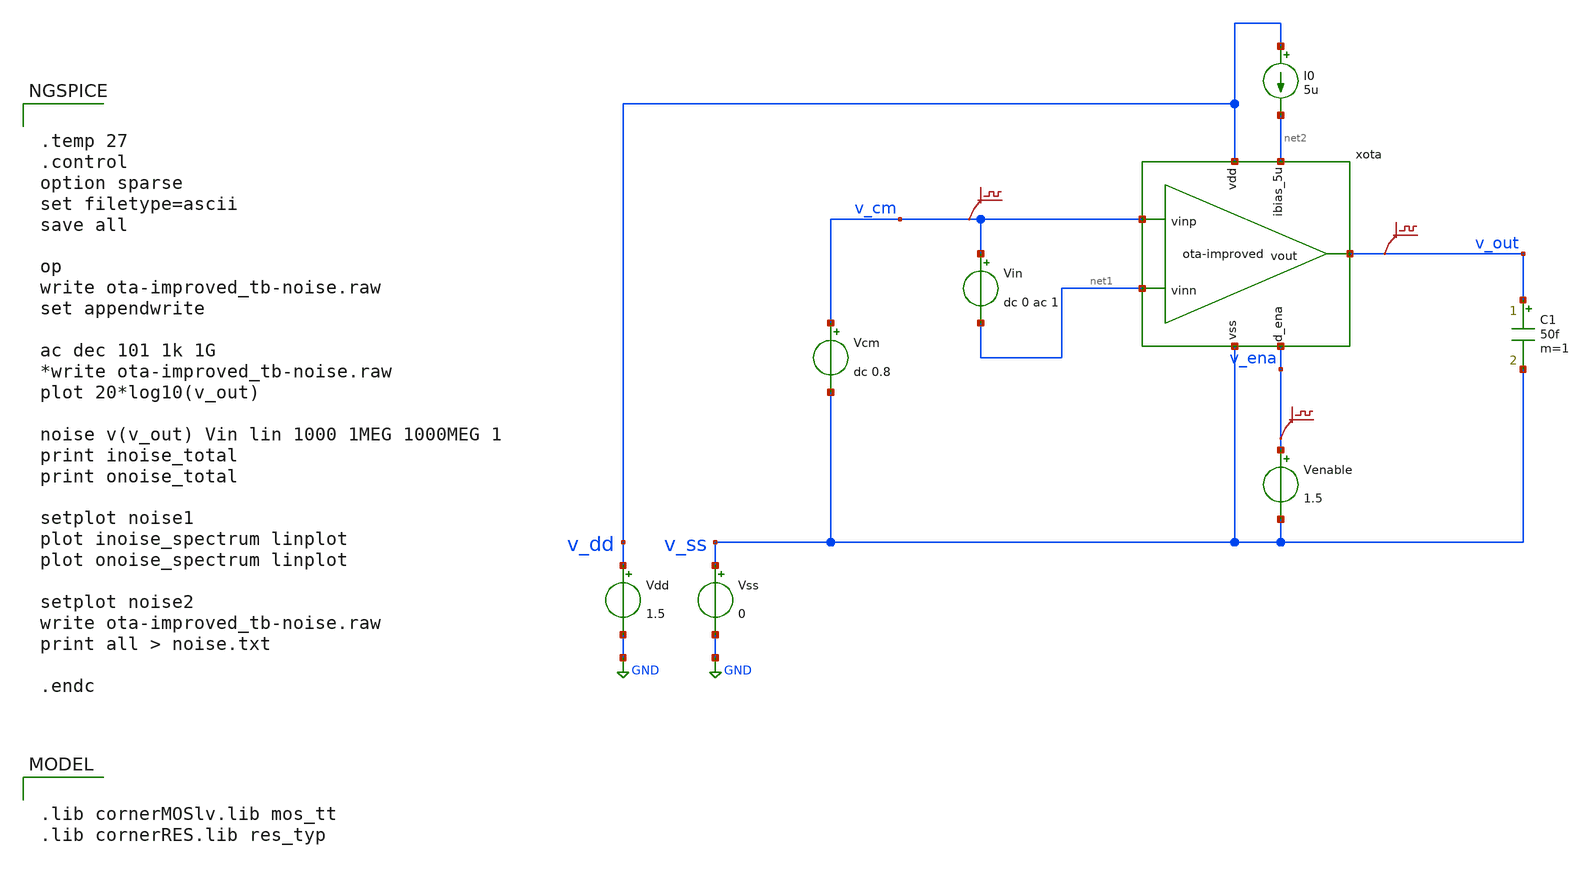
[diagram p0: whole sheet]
** sch_path: xschem/ota-improved_tb-noise.sch
* (c) 2024-2025 Harald Pretl, Apache-2.0 license
**.subckt ota-improved_tb-noise
Vdd v_dd GND 1.5
xota v_dd v_out v_cm net1 net2 v_ena v_ss ota-improved
Vss v_ss GND 0
C1 v_out v_ss 50f m=1
Vcm v_cm v_ss dc 0.8
I0 v_dd net2 5u
Venable v_ena v_ss 1.5
.save v(v_cm)
.save v(v_out)
.save v(v_ena)
Vin v_cm net1 dc 0 ac 1
**** begin user architecture code

.lib cornerMOSlv.lib mos_tt
.lib cornerRES.lib res_typ



.temp 27
.control
option sparse
set filetype=ascii
save all

op
write ota-improved_tb-noise.raw
set appendwrite

ac dec 101 1k 1G
*write ota-improved_tb-noise.raw
plot 20*log10(v_out)

noise v(v_out) Vin lin 1000 1MEG 1000MEG 1
print inoise_total
print onoise_total

setplot noise1
plot inoise_spectrum linplot
plot onoise_spectrum linplot

setplot noise2
write ota-improved_tb-noise.raw
print all > noise.txt

.endc


**** end user architecture code
**.ends

* expanding   symbol:  ota-improved.sym # of pins=7
** sym_path: xschem/ota-improved.sym
** sch_path: xschem/ota-improved.sch
.subckt ota-improved vdd vout vinp vinn ibias_5u d_ena vss
*.ipin ibias_5u
*.iopin vdd
*.iopin vss
*.ipin vinp
*.ipin vinn
*.opin vout
*.ipin d_ena
XM5 net7 gate vss vss sg13_lv_nmos w=6u l=5u ng=3 m=1 mm_ok=1
XM4 net2 gate_p vdd vdd sg13_lv_pmos w=3u l=0.5u ng=1 m=1 mm_ok=1
XM1 net5 vinp tail vss sg13_lv_nmos w=1u l=0.5u ng=1 m=1 mm_ok=1
XM2 net6 vinn tail vss sg13_lv_nmos w=1u l=0.5u ng=1 m=1 mm_ok=1
XM3 net3 gate_p vdd vdd sg13_lv_pmos w=3u l=0.5u ng=1 m=1 mm_ok=1
XM6 net1 gate vss vss sg13_lv_nmos w=2u l=5u ng=1 m=1 mm_ok=1
XMpd5 gate ena_n vss vss sg13_lv_nmos w=1u l=0.13u ng=1 m=1 mm_ok=1
XMpd3 ena ena_n vss vss sg13_lv_nmos w=1u l=0.13u ng=1 m=1 mm_ok=1
XMpd4 ena ena_n vdd vdd sg13_lv_pmos w=1u l=0.13u ng=1 m=1 mm_ok=1
XMpd6 net1 ena gate vss sg13_lv_nmos w=1u l=0.13u ng=1 m=1 mm_ok=1
XM2c vout dp_casc net6 vss sg13_lv_nmos w=1u l=0.5u ng=1 m=1 mm_ok=1
XM1c gate_p dp_casc net5 vss sg13_lv_nmos w=1u l=0.5u ng=1 m=1 mm_ok=1
XM4c vout gate_pc net2 vdd sg13_lv_pmos w=3u l=0.5u ng=1 m=1 mm_ok=1
XM3c gate_p gate_pc net3 vdd sg13_lv_pmos w=3u l=0.5u ng=1 m=1 mm_ok=1
XM7 net4 gate vss vss sg13_lv_nmos w=2u l=5u ng=1 m=1 mm_ok=1
XMpd8 gate_p ena vdd vdd sg13_lv_pmos w=1u l=0.13u ng=1 m=1 mm_ok=1
XM8_1 net8 gate_pc vdd vdd sg13_lv_pmos w=3u l=0.5u ng=1 m=1 mm_ok=1
XM9_1 net9 gate_pc vdd vdd sg13_lv_pmos w=3u l=0.5u ng=1 m=1 mm_ok=1
XMpd7 gate_pc ena vdd vdd sg13_lv_pmos w=1u l=0.13u ng=1 m=1 mm_ok=1
XM10_3 net10 dp_casc net11 vss sg13_lv_nmos w=1u l=0.5u ng=1 m=1 mm_ok=1
Vmeas gate_pc net4 0
.save i(vmeas)
Vmeas1 tail net7 0
.save i(vmeas1)
XMpd1 ena_n d_ena vss vss sg13_lv_nmos w=1u l=0.13u ng=1 m=1 mm_ok=1
XMpd2 ena_n d_ena vdd vdd sg13_lv_pmos w=1u l=0.13u ng=1 m=1 mm_ok=1
Vmeas4 ibias_5u net1 0
.save i(vmeas4)
XMpd11 vout ena_n vss vss sg13_lv_nmos w=0.5u l=0.13u ng=1 m=1 mm_ok=1
XM10_4 net11 dp_casc tail vss sg13_lv_nmos w=1u l=0.5u ng=1 m=1 mm_ok=1
XMdecoup1 vss gate vss vss sg13_lv_nmos w=8u l=1u ng=4 m=1 mm_ok=1
XMdecoup3 vdd gate_pc vdd vdd sg13_lv_pmos w=12u l=0.5u ng=4 m=1 mm_ok=1
XM10_2 net12 dp_casc net10 vss sg13_lv_nmos w=1u l=0.5u ng=1 m=1 mm_ok=1
XM10_1 dp_casc dp_casc net12 vss sg13_lv_nmos w=1u l=0.5u ng=1 m=1 mm_ok=1
XM8_2 net13 gate_pc net8 vdd sg13_lv_pmos w=3u l=0.5u ng=1 m=1 mm_ok=1
XM8_3 net14 gate_pc net13 vdd sg13_lv_pmos w=3u l=0.5u ng=1 m=1 mm_ok=1
XM9_2 net15 gate_pc net9 vdd sg13_lv_pmos w=3u l=0.5u ng=1 m=1 mm_ok=1
XM9_3 net16 gate_pc net15 vdd sg13_lv_pmos w=3u l=0.5u ng=1 m=1 mm_ok=1
XM8_4 gate_pc gate_pc net14 vdd sg13_lv_pmos w=3u l=0.5u ng=1 m=1 mm_ok=1
XM9_4 dp_casc gate_pc net16 vdd sg13_lv_pmos w=3u l=0.5u ng=1 m=1 mm_ok=1
.ends

.GLOBAL GND
.end
